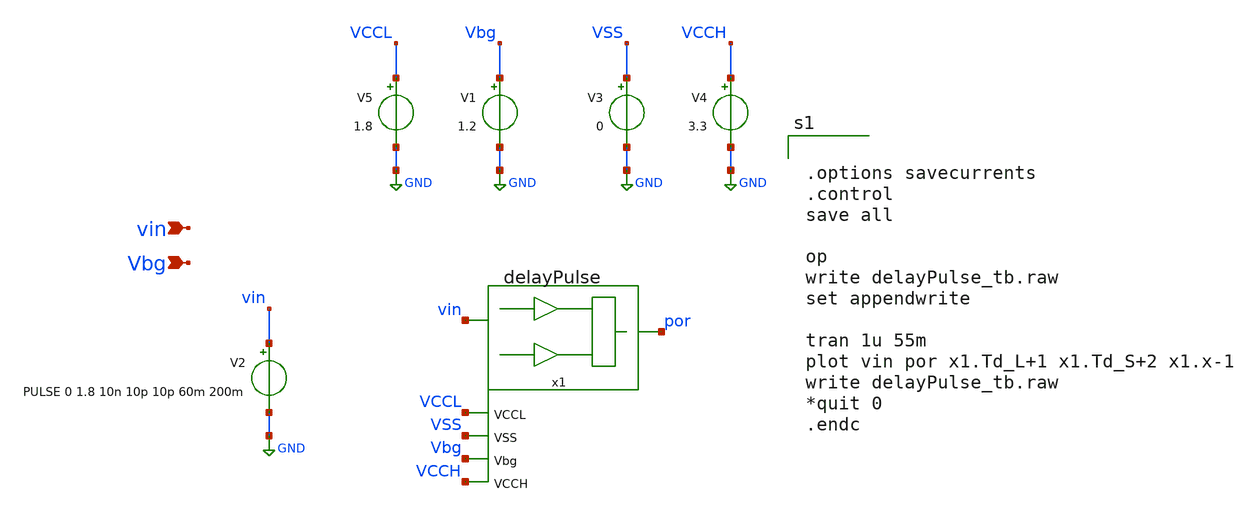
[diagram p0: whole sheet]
** sch_path: xschem/delayPulse_tb.sch
**.subckt delayPulse_tb vin Vbg
*.ipin vin
*.ipin Vbg
x1 vin por VCCL VSS Vbg VCCH delayPulse
V5 VCCL GND 1.8
V1 Vbg GND 1.2
V2 vin GND PULSE 0 1.8 10n 10p 10p 60m 200m
V3 VSS GND 0
V4 VCCH GND 3.3
**** begin user architecture code


.options savecurrents
.control
save all

op
write delayPulse_tb.raw
set appendwrite

tran 1u 55m
plot vin por x1.Td_L+1 x1.Td_S+2 x1.x-1
write delayPulse_tb.raw
*quit 0
.endc


 .lib $::SKYWATER_MODELS/sky130.lib.spice tt

.include $::SKYWATER_STDCELLS/sky130_fd_sc_hd.spice

**** end user architecture code
**.ends
.GLOBAL GND
.end
